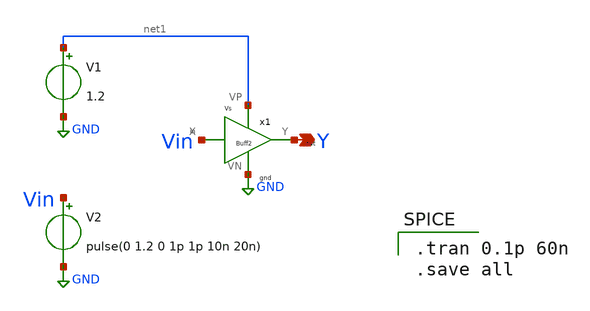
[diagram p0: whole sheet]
** sch_path: Blocks/Buffer/Buff_sym_test.sch
**.subckt Buff_sym_test Y
*.opin Y
x1 Vin Y net1 GND Buff
V1 net1 GND 1.2
V2 Vin GND pulse(0 1.2 0 1p 1p 10n 20n)
**** begin user architecture code

** opencircuitdesign pdks install
.lib $::SKYWATER_MODELS/sky130.lib.spice tt



.tran 0.1p 60n
.save all

**** end user architecture code
**.ends

* expanding   symbol:  PICO_project/Buffer/Buff.sym # of pins=4
** sym_path: Blocks/Buffer/Buff.sym
** sch_path: Blocks/Buffer/Buff.sch
.subckt Buff X Y VP VN
*.ipin X
*.opin Y
*.iopin VN
*.iopin VP
x1 X net1 VP VN INV
x2 net1 Y VP VN INV
.ends


* expanding   symbol:  Pico_project/INV/INV.sym # of pins=4
** sym_path: component/INV/INV.sym
** sch_path: component/INV/INV.sch
.subckt INV X Y VP VN
*.ipin X
*.opin Y
*.iopin VN
*.iopin VP
XM1 Y X VN VN sky130_fd_pr__nfet_01v8 L=0.15 W=0.42 nf=1 ad='int((nf+1)/2) * W/nf * 0.29' as='int((nf+2)/2) * W/nf * 0.29'
+ pd='2*int((nf+1)/2) * (W/nf + 0.29)' ps='2*int((nf+2)/2) * (W/nf + 0.29)' nrd='0.29 / W' nrs='0.29 / W'
+ sa=0 sb=0 sd=0 mult=1 m=1
XM2 Y X VP VP sky130_fd_pr__pfet_01v8 L=0.15 W=1.26 nf=1 ad='int((nf+1)/2) * W/nf * 0.29' as='int((nf+2)/2) * W/nf * 0.29'
+ pd='2*int((nf+1)/2) * (W/nf + 0.29)' ps='2*int((nf+2)/2) * (W/nf + 0.29)' nrd='0.29 / W' nrs='0.29 / W'
+ sa=0 sb=0 sd=0 mult=1 m=1
.ends

.GLOBAL GND
.end
